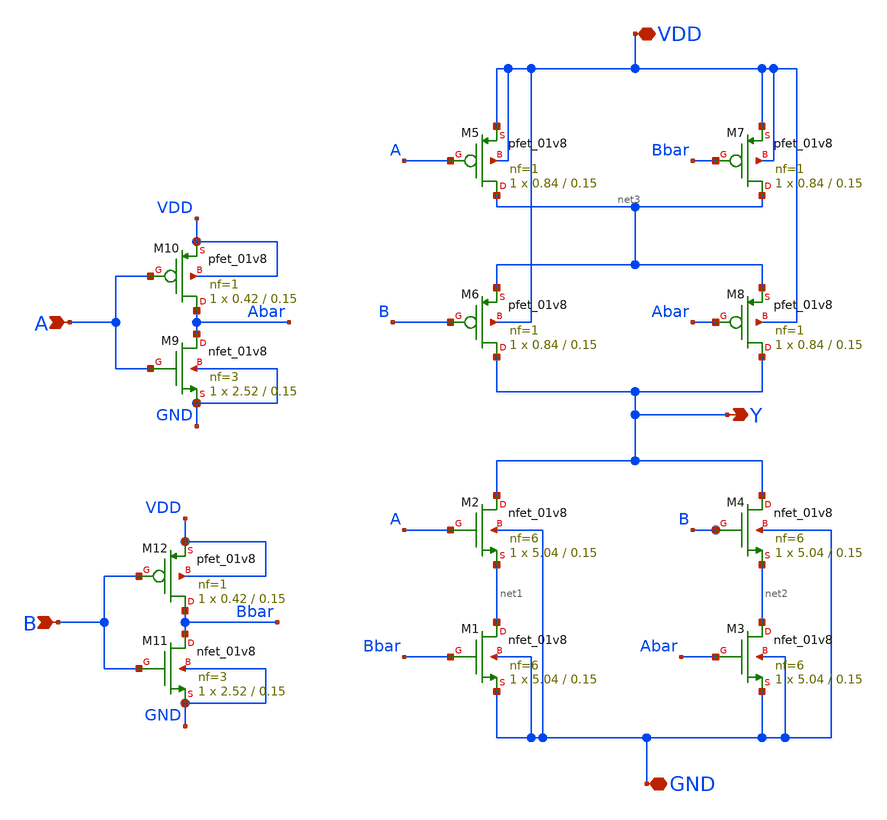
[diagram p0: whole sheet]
** sch_path: cells/XNOR2X1/schematic/xnor2x1.sch
**.subckt xnor2x1 A B Y VDD GND
*.ipin A
*.ipin B
*.opin Y
*.iopin VDD
*.iopin GND
XM9 Abar A GND GND sky130_fd_pr__nfet_01v8 L=0.15 W=2.52 nf=3 ad='int((3 + 1)/2) * 2.52 / 3 * 0.29' as='int((3 + 2)/2) * 2.52 / 3 * 0.29'
+ pd='2*int((3 + 1)/2) * (2.52 / 3 + 0.29)' ps='2*int((3 + 2)/2) * (2.52 / 3 + 0.29)' nrd='0.29 / 2.52 '
+ nrs='0.29 / 2.52 ' sa=0 sb=0 sd=0 mult=1 m=1
XM10 Abar A VDD VDD sky130_fd_pr__pfet_01v8 L=0.15 W=0.42 nf=1 ad='int((1 + 1)/2) * 0.42 / 1 * 0.29'
+ as='int((1 + 2)/2) * 0.42 / 1 * 0.29' pd='2*int((1 + 1)/2) * (0.42 / 1 + 0.29)' ps='2*int((1 + 2)/2) * (0.42 / 1 + 0.29)'
+ nrd='0.29 / 0.42 ' nrs='0.29 / 0.42 ' sa=0 sb=0 sd=0 mult=1 m=1
XM2 Y A net1 GND sky130_fd_pr__nfet_01v8 L=0.15 W=5.04 nf=6 ad='int((6 + 1)/2) * 5.04 / 6 * 0.29' as='int((6 + 2)/2) * 5.04 / 6 * 0.29'
+ pd='2*int((6 + 1)/2) * (5.04 / 6 + 0.29)' ps='2*int((6 + 2)/2) * (5.04 / 6 + 0.29)' nrd='0.29 / 5.04 '
+ nrs='0.29 / 5.04 ' sa=0 sb=0 sd=0 mult=1 m=1
XM5 net3 A VDD VDD sky130_fd_pr__pfet_01v8 L=0.15 W=0.84 nf=1 ad='int((1 + 1)/2) * 0.84 / 1 * 0.29' as='int((1 + 2)/2) * 0.84 / 1 * 0.29'
+ pd='2*int((1 + 1)/2) * (0.84 / 1 + 0.29)' ps='2*int((1 + 2)/2) * (0.84 / 1 + 0.29)' nrd='0.29 / 0.84 '
+ nrs='0.29 / 0.84 ' sa=0 sb=0 sd=0 mult=1 m=1
XM12 Bbar B VDD VDD sky130_fd_pr__pfet_01v8 L=0.15 W=0.42 nf=1 ad='int((1 + 1)/2) * 0.42 / 1 * 0.29'
+ as='int((1 + 2)/2) * 0.42 / 1 * 0.29' pd='2*int((1 + 1)/2) * (0.42 / 1 + 0.29)' ps='2*int((1 + 2)/2) * (0.42 / 1 + 0.29)'
+ nrd='0.29 / 0.42 ' nrs='0.29 / 0.42 ' sa=0 sb=0 sd=0 mult=1 m=1
XM11 Bbar B GND GND sky130_fd_pr__nfet_01v8 L=0.15 W=2.52 nf=3 ad='int((3 + 1)/2) * 2.52 / 3 * 0.29'
+ as='int((3 + 2)/2) * 2.52 / 3 * 0.29' pd='2*int((3 + 1)/2) * (2.52 / 3 + 0.29)' ps='2*int((3 + 2)/2) * (2.52 / 3 + 0.29)'
+ nrd='0.29 / 2.52 ' nrs='0.29 / 2.52 ' sa=0 sb=0 sd=0 mult=1 m=1
XM1 net1 Bbar GND GND sky130_fd_pr__nfet_01v8 L=0.15 W=5.04 nf=6 ad='int((6 + 1)/2) * 5.04 / 6 * 0.29'
+ as='int((6 + 2)/2) * 5.04 / 6 * 0.29' pd='2*int((6 + 1)/2) * (5.04 / 6 + 0.29)' ps='2*int((6 + 2)/2) * (5.04 / 6 + 0.29)'
+ nrd='0.29 / 5.04 ' nrs='0.29 / 5.04 ' sa=0 sb=0 sd=0 mult=1 m=1
XM3 net2 Abar GND GND sky130_fd_pr__nfet_01v8 L=0.15 W=5.04 nf=6 ad='int((6 + 1)/2) * 5.04 / 6 * 0.29'
+ as='int((6 + 2)/2) * 5.04 / 6 * 0.29' pd='2*int((6 + 1)/2) * (5.04 / 6 + 0.29)' ps='2*int((6 + 2)/2) * (5.04 / 6 + 0.29)'
+ nrd='0.29 / 5.04 ' nrs='0.29 / 5.04 ' sa=0 sb=0 sd=0 mult=1 m=1
XM4 Y B net2 GND sky130_fd_pr__nfet_01v8 L=0.15 W=5.04 nf=6 ad='int((6 + 1)/2) * 5.04 / 6 * 0.29' as='int((6 + 2)/2) * 5.04 / 6 * 0.29'
+ pd='2*int((6 + 1)/2) * (5.04 / 6 + 0.29)' ps='2*int((6 + 2)/2) * (5.04 / 6 + 0.29)' nrd='0.29 / 5.04 '
+ nrs='0.29 / 5.04 ' sa=0 sb=0 sd=0 mult=1 m=1
XM6 Y B net3 VDD sky130_fd_pr__pfet_01v8 L=0.15 W=0.84 nf=1 ad='int((1 + 1)/2) * 0.84 / 1 * 0.29' as='int((1 + 2)/2) * 0.84 / 1 * 0.29'
+ pd='2*int((1 + 1)/2) * (0.84 / 1 + 0.29)' ps='2*int((1 + 2)/2) * (0.84 / 1 + 0.29)' nrd='0.29 / 0.84 '
+ nrs='0.29 / 0.84 ' sa=0 sb=0 sd=0 mult=1 m=1
XM8 Y Abar net3 VDD sky130_fd_pr__pfet_01v8 L=0.15 W=0.84 nf=1 ad='int((1 + 1)/2) * 0.84 / 1 * 0.29'
+ as='int((1 + 2)/2) * 0.84 / 1 * 0.29' pd='2*int((1 + 1)/2) * (0.84 / 1 + 0.29)' ps='2*int((1 + 2)/2) * (0.84 / 1 + 0.29)'
+ nrd='0.29 / 0.84 ' nrs='0.29 / 0.84 ' sa=0 sb=0 sd=0 mult=1 m=1
XM7 net3 Bbar VDD VDD sky130_fd_pr__pfet_01v8 L=0.15 W=0.84 nf=1 ad='int((1 + 1)/2) * 0.84 / 1 * 0.29'
+ as='int((1 + 2)/2) * 0.84 / 1 * 0.29' pd='2*int((1 + 1)/2) * (0.84 / 1 + 0.29)' ps='2*int((1 + 2)/2) * (0.84 / 1 + 0.29)'
+ nrd='0.29 / 0.84 ' nrs='0.29 / 0.84 ' sa=0 sb=0 sd=0 mult=1 m=1
**.ends
.end
